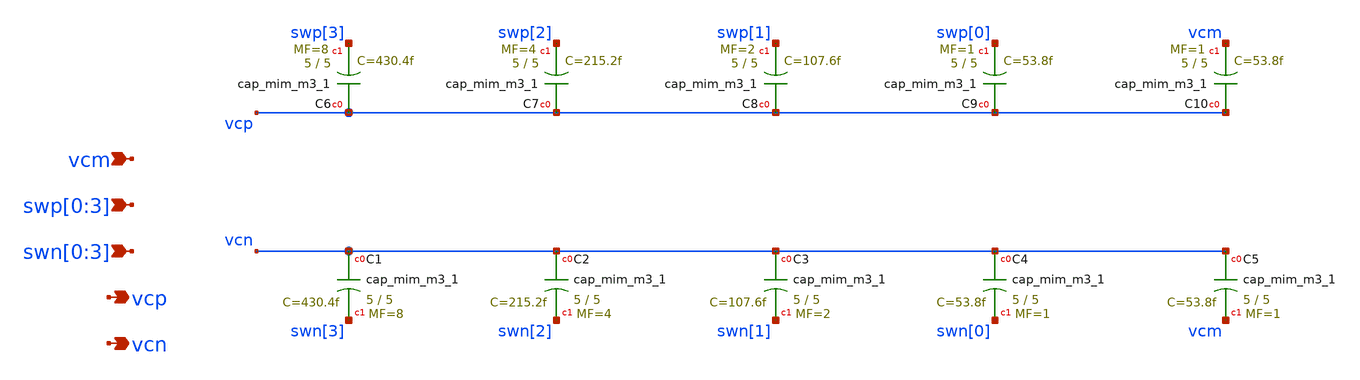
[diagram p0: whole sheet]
** sch_path: xschem/4b_cdac.sch
**.subckt 4b_cdac vcm swp[0],swp[1],swp[2],swp[3] swn[0],swn[1],swn[2],swn[3] vcp vcn
*.ipin vcm
*.ipin swp[0],swp[1],swp[2],swp[3]
*.ipin swn[0],swn[1],swn[2],swn[3]
*.opin vcp
*.opin vcn
XC1 vcn swn[3] sky130_fd_pr__cap_mim_m3_1 W=5 L=5 MF=8 m=8
XC2 vcn swn[2] sky130_fd_pr__cap_mim_m3_1 W=5 L=5 MF=4 m=4
XC3 vcn swn[1] sky130_fd_pr__cap_mim_m3_1 W=5 L=5 MF=2 m=2
XC4 vcn swn[0] sky130_fd_pr__cap_mim_m3_1 W=5 L=5 MF=1 m=1
XC5 vcn vcm sky130_fd_pr__cap_mim_m3_1 W=5 L=5 MF=1 m=1
XC6 vcp swp[3] sky130_fd_pr__cap_mim_m3_1 W=5 L=5 MF=8 m=8
XC7 vcp swp[2] sky130_fd_pr__cap_mim_m3_1 W=5 L=5 MF=4 m=4
XC8 vcp swp[1] sky130_fd_pr__cap_mim_m3_1 W=5 L=5 MF=2 m=2
XC9 vcp swp[0] sky130_fd_pr__cap_mim_m3_1 W=5 L=5 MF=1 m=1
XC10 vcp vcm sky130_fd_pr__cap_mim_m3_1 W=5 L=5 MF=1 m=1
**.ends
.end
